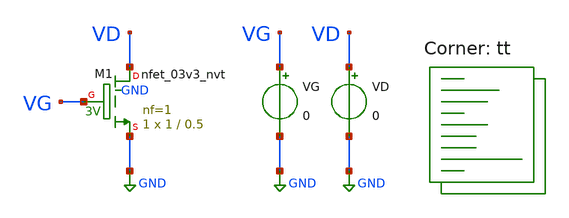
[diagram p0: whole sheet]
** sch_path: week01_mosfet_cmos/tugas1_iv_curve/nfet_iv_curve.sch
**.subckt nfet_iv_curve
XM1 VD VG GND GND sky130_fd_pr__nfet_03v3_nvt L=0.5 W=1 nf=1 ad='int((nf+1)/2) * W/nf * 0.29' as='int((nf+2)/2) * W/nf * 0.29'
+ pd='2*int((nf+1)/2) * (W/nf + 0.29)' ps='2*int((nf+2)/2) * (W/nf + 0.29)' nrd='0.29 / W' nrs='0.29 / W'
+ sa=0 sb=0 sd=0 mult=1 m=1
VG VG GND 0
VD VD GND 0
**** begin user architecture code
.lib $::SKYWATER_MODELS/sky130.lib.spice tt


.control
	dc VD 0 3.3 0.1 VG 0 3.3 0.33
	plot -i(VD)
saveall
.endc


**** end user architecture code
**.ends
.GLOBAL GND
.end
